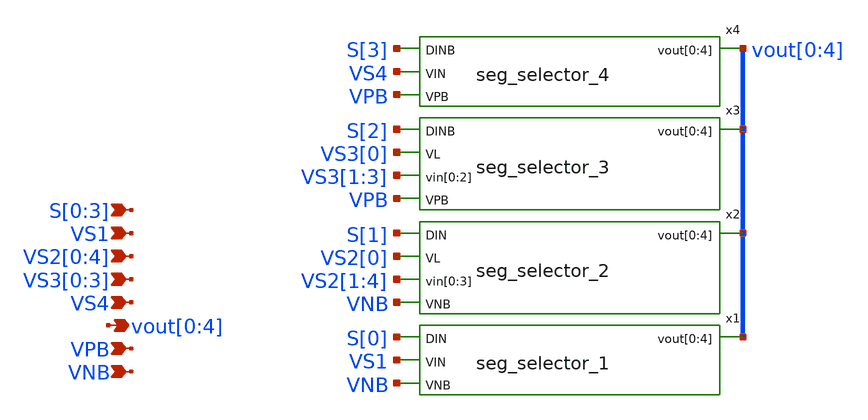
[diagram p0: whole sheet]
** sch_path: xschem/seg_selector.sch
**.subckt seg_selector vout[0],vout[1],vout[2],vout[3],vout[4] VNB VPB S[0],S[1],S[2],S[3] VS1
*+ VS2[0],VS2[1],VS2[2],VS2[3],VS2[4] VS3[0],VS3[1],VS3[2],VS3[3] VS4
*.opin vout[0],vout[1],vout[2],vout[3],vout[4]
*.ipin VNB
*.ipin VPB
*.ipin S[0],S[1],S[2],S[3]
*.ipin VS1
*.ipin VS2[0],VS2[1],VS2[2],VS2[3],VS2[4]
*.ipin VS3[0],VS3[1],VS3[2],VS3[3]
*.ipin VS4
x1 S[0] VS1 vout[0] vout[1] vout[2] vout[3] vout[4] VNB seg_selector_1
x2 S[1] VS2[0] VS2[1] VS2[2] VS2[3] VS2[4] vout[0] vout[1] vout[2] vout[3] vout[4] VNB
+ seg_selector_2
x3 S[2] VS3[0] VS3[1] VS3[2] VS3[3] vout[0] vout[1] vout[2] vout[3] vout[4] VPB seg_selector_3
x4 S[3] VS4 vout[0] vout[1] vout[2] vout[3] vout[4] VPB seg_selector_4
**.ends

* expanding   symbol:  seg_selector_1.sym # of pins=4
** sym_path: xschem/seg_selector_1.sym
** sch_path: xschem/seg_selector_1.sch
.subckt seg_selector_1 DIN VIN vout[0] vout[1] vout[2] vout[3] vout[4] VNB
*.opin vout[0],vout[1],vout[2],vout[3],vout[4]
*.ipin VNB
*.ipin DIN
*.ipin VIN
.param wp=0.42 wn=0.42 l=0.5

XM1 vout[0] DIN VIN VNB sky130_fd_pr__nfet_g5v0d10v5 L=l W=wn nf=1 ad='int((nf+1)/2) * W/nf * 0.29' as='int((nf+2)/2) * W/nf * 0.29'
+ pd='2*int((nf+1)/2) * (W/nf + 0.29)' ps='2*int((nf+2)/2) * (W/nf + 0.29)' nrd='0.29 / W' nrs='0.29 / W'
+ sa=0 sb=0 sd=0 mult=1 m=1
XM2 vout[1] DIN VIN VNB sky130_fd_pr__nfet_g5v0d10v5 L=l W=wn nf=1 ad='int((nf+1)/2) * W/nf * 0.29' as='int((nf+2)/2) * W/nf * 0.29'
+ pd='2*int((nf+1)/2) * (W/nf + 0.29)' ps='2*int((nf+2)/2) * (W/nf + 0.29)' nrd='0.29 / W' nrs='0.29 / W'
+ sa=0 sb=0 sd=0 mult=1 m=1
XM3 vout[2] DIN VIN VNB sky130_fd_pr__nfet_g5v0d10v5 L=l W=wn nf=1 ad='int((nf+1)/2) * W/nf * 0.29' as='int((nf+2)/2) * W/nf * 0.29'
+ pd='2*int((nf+1)/2) * (W/nf + 0.29)' ps='2*int((nf+2)/2) * (W/nf + 0.29)' nrd='0.29 / W' nrs='0.29 / W'
+ sa=0 sb=0 sd=0 mult=1 m=1
XM4 vout[3] DIN VIN VNB sky130_fd_pr__nfet_g5v0d10v5 L=l W=wn nf=1 ad='int((nf+1)/2) * W/nf * 0.29' as='int((nf+2)/2) * W/nf * 0.29'
+ pd='2*int((nf+1)/2) * (W/nf + 0.29)' ps='2*int((nf+2)/2) * (W/nf + 0.29)' nrd='0.29 / W' nrs='0.29 / W'
+ sa=0 sb=0 sd=0 mult=1 m=1
XM5 vout[4] DIN VIN VNB sky130_fd_pr__nfet_g5v0d10v5 L=l W=wn nf=1 ad='int((nf+1)/2) * W/nf * 0.29' as='int((nf+2)/2) * W/nf * 0.29'
+ pd='2*int((nf+1)/2) * (W/nf + 0.29)' ps='2*int((nf+2)/2) * (W/nf + 0.29)' nrd='0.29 / W' nrs='0.29 / W'
+ sa=0 sb=0 sd=0 mult=1 m=1
.ends


* expanding   symbol:  seg_selector_2.sym # of pins=5
** sym_path: xschem/seg_selector_2.sym
** sch_path: xschem/seg_selector_2.sch
.subckt seg_selector_2 DIN VL vin[0] vin[1] vin[2] vin[3] vout[0] vout[1] vout[2] vout[3] vout[4]
+ VNB
*.opin vout[0],vout[1],vout[2],vout[3],vout[4]
*.ipin VNB
*.ipin DIN
*.ipin vin[0],vin[1],vin[2],vin[3]
*.ipin VL
.param wp=0.42 wn=0.42 l=0.5

XM1 vout[0] DIN VL VNB sky130_fd_pr__nfet_g5v0d10v5 L=l W=wn nf=1 ad='int((nf+1)/2) * W/nf * 0.29' as='int((nf+2)/2) * W/nf * 0.29'
+ pd='2*int((nf+1)/2) * (W/nf + 0.29)' ps='2*int((nf+2)/2) * (W/nf + 0.29)' nrd='0.29 / W' nrs='0.29 / W'
+ sa=0 sb=0 sd=0 mult=1 m=1
XM2 vout[1] DIN vin[0] VNB sky130_fd_pr__nfet_g5v0d10v5 L=l W=wn nf=1 ad='int((nf+1)/2) * W/nf * 0.29'
+ as='int((nf+2)/2) * W/nf * 0.29' pd='2*int((nf+1)/2) * (W/nf + 0.29)' ps='2*int((nf+2)/2) * (W/nf + 0.29)'
+ nrd='0.29 / W' nrs='0.29 / W' sa=0 sb=0 sd=0 mult=1 m=1
XM3 vout[2] DIN vin[1] VNB sky130_fd_pr__nfet_g5v0d10v5 L=l W=wn nf=1 ad='int((nf+1)/2) * W/nf * 0.29'
+ as='int((nf+2)/2) * W/nf * 0.29' pd='2*int((nf+1)/2) * (W/nf + 0.29)' ps='2*int((nf+2)/2) * (W/nf + 0.29)'
+ nrd='0.29 / W' nrs='0.29 / W' sa=0 sb=0 sd=0 mult=1 m=1
XM4 vout[3] DIN vin[2] VNB sky130_fd_pr__nfet_g5v0d10v5 L=l W=wn nf=1 ad='int((nf+1)/2) * W/nf * 0.29'
+ as='int((nf+2)/2) * W/nf * 0.29' pd='2*int((nf+1)/2) * (W/nf + 0.29)' ps='2*int((nf+2)/2) * (W/nf + 0.29)'
+ nrd='0.29 / W' nrs='0.29 / W' sa=0 sb=0 sd=0 mult=1 m=1
XM5 vout[4] DIN vin[3] VNB sky130_fd_pr__nfet_g5v0d10v5 L=l W=wn nf=1 ad='int((nf+1)/2) * W/nf * 0.29'
+ as='int((nf+2)/2) * W/nf * 0.29' pd='2*int((nf+1)/2) * (W/nf + 0.29)' ps='2*int((nf+2)/2) * (W/nf + 0.29)'
+ nrd='0.29 / W' nrs='0.29 / W' sa=0 sb=0 sd=0 mult=1 m=1
.ends


* expanding   symbol:  seg_selector_3.sym # of pins=5
** sym_path: xschem/seg_selector_3.sym
** sch_path: xschem/seg_selector_3.sch
.subckt seg_selector_3 DINB VL vin[0] vin[1] vin[2] vout[0] vout[1] vout[2] vout[3] vout[4] VPB
*.opin vout[0],vout[1],vout[2],vout[3],vout[4]
*.ipin VPB
*.ipin DINB
*.ipin vin[0],vin[1],vin[2]
*.ipin VL
.param wp=0.42 wn=0.42 l=0.5

XM1 vout[0] DINB VL VPB sky130_fd_pr__pfet_g5v0d10v5 L=l W=wp nf=1 ad='int((nf+1)/2) * W/nf * 0.29' as='int((nf+2)/2) * W/nf * 0.29'
+ pd='2*int((nf+1)/2) * (W/nf + 0.29)' ps='2*int((nf+2)/2) * (W/nf + 0.29)' nrd='0.29 / W' nrs='0.29 / W'
+ sa=0 sb=0 sd=0 mult=1 m=1
XM2 vout[1] DINB VL VPB sky130_fd_pr__pfet_g5v0d10v5 L=l W=wp nf=1 ad='int((nf+1)/2) * W/nf * 0.29' as='int((nf+2)/2) * W/nf * 0.29'
+ pd='2*int((nf+1)/2) * (W/nf + 0.29)' ps='2*int((nf+2)/2) * (W/nf + 0.29)' nrd='0.29 / W' nrs='0.29 / W'
+ sa=0 sb=0 sd=0 mult=1 m=1
XM3 vout[2] DINB vin[0] VPB sky130_fd_pr__pfet_g5v0d10v5 L=l W=wp nf=1 ad='int((nf+1)/2) * W/nf * 0.29'
+ as='int((nf+2)/2) * W/nf * 0.29' pd='2*int((nf+1)/2) * (W/nf + 0.29)' ps='2*int((nf+2)/2) * (W/nf + 0.29)'
+ nrd='0.29 / W' nrs='0.29 / W' sa=0 sb=0 sd=0 mult=1 m=1
XM4 vout[3] DINB vin[1] VPB sky130_fd_pr__pfet_g5v0d10v5 L=l W=wp nf=1 ad='int((nf+1)/2) * W/nf * 0.29'
+ as='int((nf+2)/2) * W/nf * 0.29' pd='2*int((nf+1)/2) * (W/nf + 0.29)' ps='2*int((nf+2)/2) * (W/nf + 0.29)'
+ nrd='0.29 / W' nrs='0.29 / W' sa=0 sb=0 sd=0 mult=1 m=1
XM5 vout[4] DINB vin[2] VPB sky130_fd_pr__pfet_g5v0d10v5 L=l W=wp nf=1 ad='int((nf+1)/2) * W/nf * 0.29'
+ as='int((nf+2)/2) * W/nf * 0.29' pd='2*int((nf+1)/2) * (W/nf + 0.29)' ps='2*int((nf+2)/2) * (W/nf + 0.29)'
+ nrd='0.29 / W' nrs='0.29 / W' sa=0 sb=0 sd=0 mult=1 m=1
.ends


* expanding   symbol:  seg_selector_4.sym # of pins=4
** sym_path: xschem/seg_selector_4.sym
** sch_path: xschem/seg_selector_4.sch
.subckt seg_selector_4 DINB VIN vout[0] vout[1] vout[2] vout[3] vout[4] VPB
*.opin vout[0],vout[1],vout[2],vout[3],vout[4]
*.ipin VPB
*.ipin DINB
*.ipin VIN
.param wp=0.42 wn=0.42 l=0.5

XM1 vout[0] DINB VIN VPB sky130_fd_pr__pfet_g5v0d10v5 L=l W=wp nf=1 ad='int((nf+1)/2) * W/nf * 0.29'
+ as='int((nf+2)/2) * W/nf * 0.29' pd='2*int((nf+1)/2) * (W/nf + 0.29)' ps='2*int((nf+2)/2) * (W/nf + 0.29)'
+ nrd='0.29 / W' nrs='0.29 / W' sa=0 sb=0 sd=0 mult=1 m=1
XM2 vout[1] DINB VIN VPB sky130_fd_pr__pfet_g5v0d10v5 L=l W=wp nf=1 ad='int((nf+1)/2) * W/nf * 0.29'
+ as='int((nf+2)/2) * W/nf * 0.29' pd='2*int((nf+1)/2) * (W/nf + 0.29)' ps='2*int((nf+2)/2) * (W/nf + 0.29)'
+ nrd='0.29 / W' nrs='0.29 / W' sa=0 sb=0 sd=0 mult=1 m=1
XM3 vout[2] DINB VIN VPB sky130_fd_pr__pfet_g5v0d10v5 L=l W=wp nf=1 ad='int((nf+1)/2) * W/nf * 0.29'
+ as='int((nf+2)/2) * W/nf * 0.29' pd='2*int((nf+1)/2) * (W/nf + 0.29)' ps='2*int((nf+2)/2) * (W/nf + 0.29)'
+ nrd='0.29 / W' nrs='0.29 / W' sa=0 sb=0 sd=0 mult=1 m=1
XM4 vout[3] DINB VIN VPB sky130_fd_pr__pfet_g5v0d10v5 L=l W=wp nf=1 ad='int((nf+1)/2) * W/nf * 0.29'
+ as='int((nf+2)/2) * W/nf * 0.29' pd='2*int((nf+1)/2) * (W/nf + 0.29)' ps='2*int((nf+2)/2) * (W/nf + 0.29)'
+ nrd='0.29 / W' nrs='0.29 / W' sa=0 sb=0 sd=0 mult=1 m=1
XM5 vout[4] DINB VIN VPB sky130_fd_pr__pfet_g5v0d10v5 L=l W=wp nf=1 ad='int((nf+1)/2) * W/nf * 0.29'
+ as='int((nf+2)/2) * W/nf * 0.29' pd='2*int((nf+1)/2) * (W/nf + 0.29)' ps='2*int((nf+2)/2) * (W/nf + 0.29)'
+ nrd='0.29 / W' nrs='0.29 / W' sa=0 sb=0 sd=0 mult=1 m=1
.ends

.end
